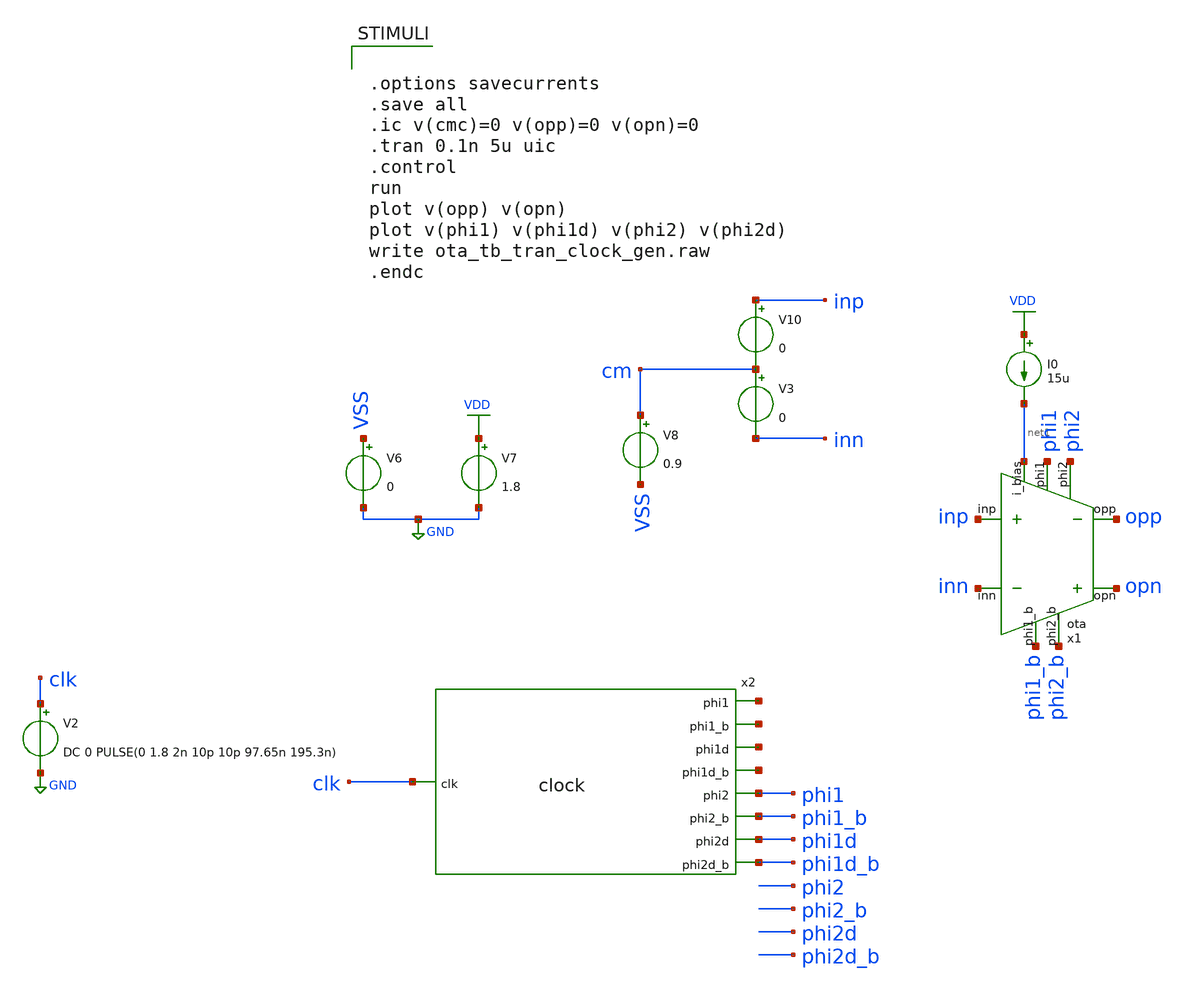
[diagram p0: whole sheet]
** sch_path: verification/schematic/ota_tb_tran_clock_gen.sch
**.subckt ota_tb_tran_clock_gen
V6 VSS GND 0
V7 VDD GND 1.8
V8 cm VSS 0.9
V10 inp cm 0
V3 cm inn 0
x1 net1 inp inn phi1 phi1_b phi2 phi2_b opp opn 50 350 VDD VSS ota
I0 VDD net1 15u
x2 clk net2 net3 net4 net5 phi1 phi1_b phi1d phi1d_b clock
V2 clk GND DC 0 PULSE(0 1.8 2n 10p 10p 97.65n 195.3n)
**** begin user architecture code

** opencircuitdesign pdks install
.lib /farmshare/home/classes/ee/372/PDKs/open_pdks_1.0.310/sky130/sky130A/libs.tech/ngspice/sky130.lib.spice tt
.include /farmshare/home/classes/ee/372/PDKs/open_pdks_1.0.310/sky130/sky130A/libs.ref/sky130_fd_sc_hd/spice/sky130_fd_sc_hd.spice



.options savecurrents
.save all
.ic v(cmc)=0 v(opp)=0 v(opn)=0
.tran 0.1n 5u uic
.control
run
plot v(opp) v(opn)
plot v(phi1) v(phi1d) v(phi2) v(phi2d)
write ota_tb_tran_clock_gen.raw
.endc


**** end user architecture code
**.ends
.GLOBAL VDD
.GLOBAL GND
.end
